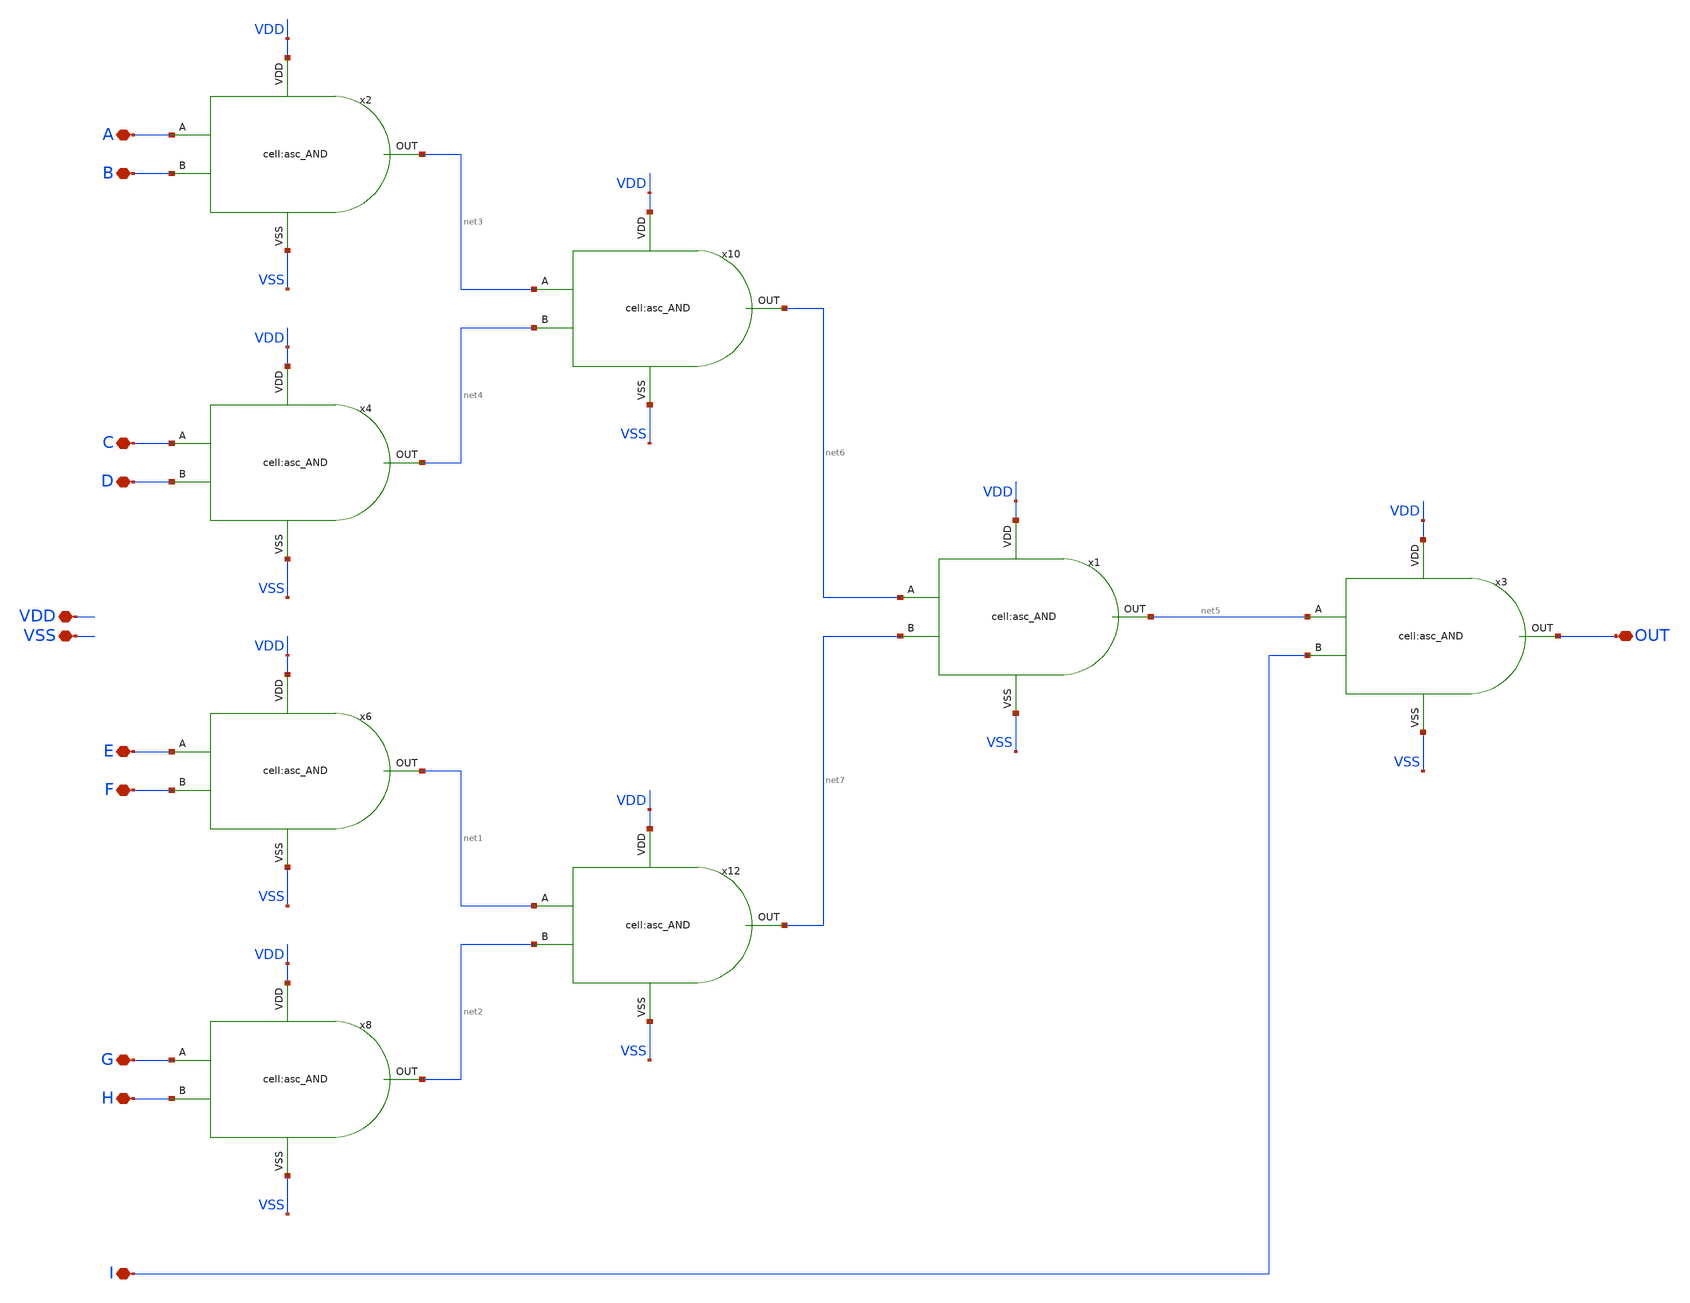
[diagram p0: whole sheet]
** sch_path: designs/libs/xp_core_analog/asc_AND_9/asc_AND_9.sch
**.subckt asc_AND_9 VDD VSS B A D C F E H G I OUT
*.iopin VDD
*.iopin VSS
*.iopin B
*.iopin A
*.iopin D
*.iopin C
*.iopin F
*.iopin E
*.iopin H
*.iopin G
*.iopin I
*.iopin OUT
x2 VDD net3 A B VSS asc_AND
x4 VDD net4 C D VSS asc_AND
x6 VDD net1 E F VSS asc_AND
x8 VDD net2 G H VSS asc_AND
x10 VDD net6 net3 net4 VSS asc_AND
x12 VDD net7 net1 net2 VSS asc_AND
x1 VDD net5 net6 net7 VSS asc_AND
x3 VDD OUT net5 I VSS asc_AND
**.ends
.end
